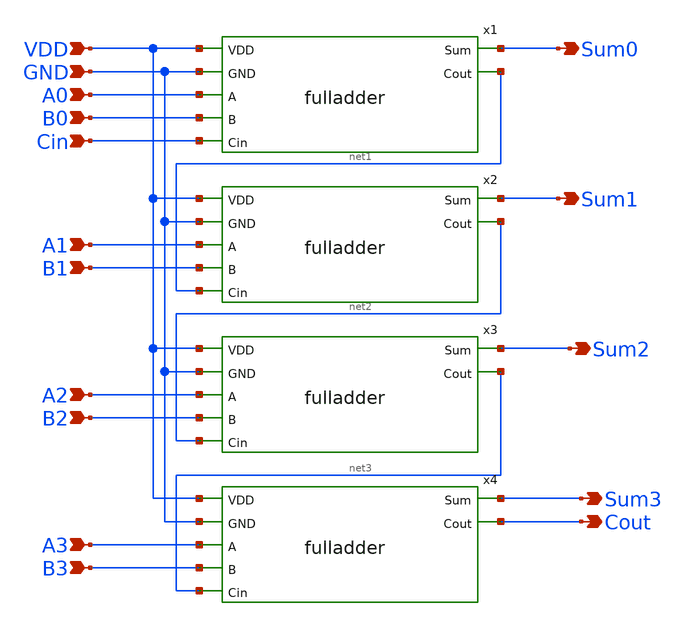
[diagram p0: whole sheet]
** sch_path: static_cmos/schematic/fulladder_4bit.sch
**.subckt fulladder_4bit A0 B0 Cin A1 B1 A2 B2 A3 B3 Sum0 Sum1 Sum2 Sum3 Cout GND VDD
*.ipin A0
*.ipin B0
*.ipin Cin
*.ipin A1
*.ipin B1
*.ipin A2
*.ipin B2
*.ipin A3
*.ipin B3
*.opin Sum0
*.opin Sum1
*.opin Sum2
*.opin Sum3
*.opin Cout
*.ipin GND
*.ipin VDD
x1 VDD GND Sum0 A0 B0 Cin net1 fulladder
x2 VDD GND Sum1 A1 B1 net1 net2 fulladder
x3 VDD GND Sum2 A2 B2 net2 net3 fulladder
x4 VDD GND Sum3 A3 B3 net3 Cout fulladder
**.ends
.end
